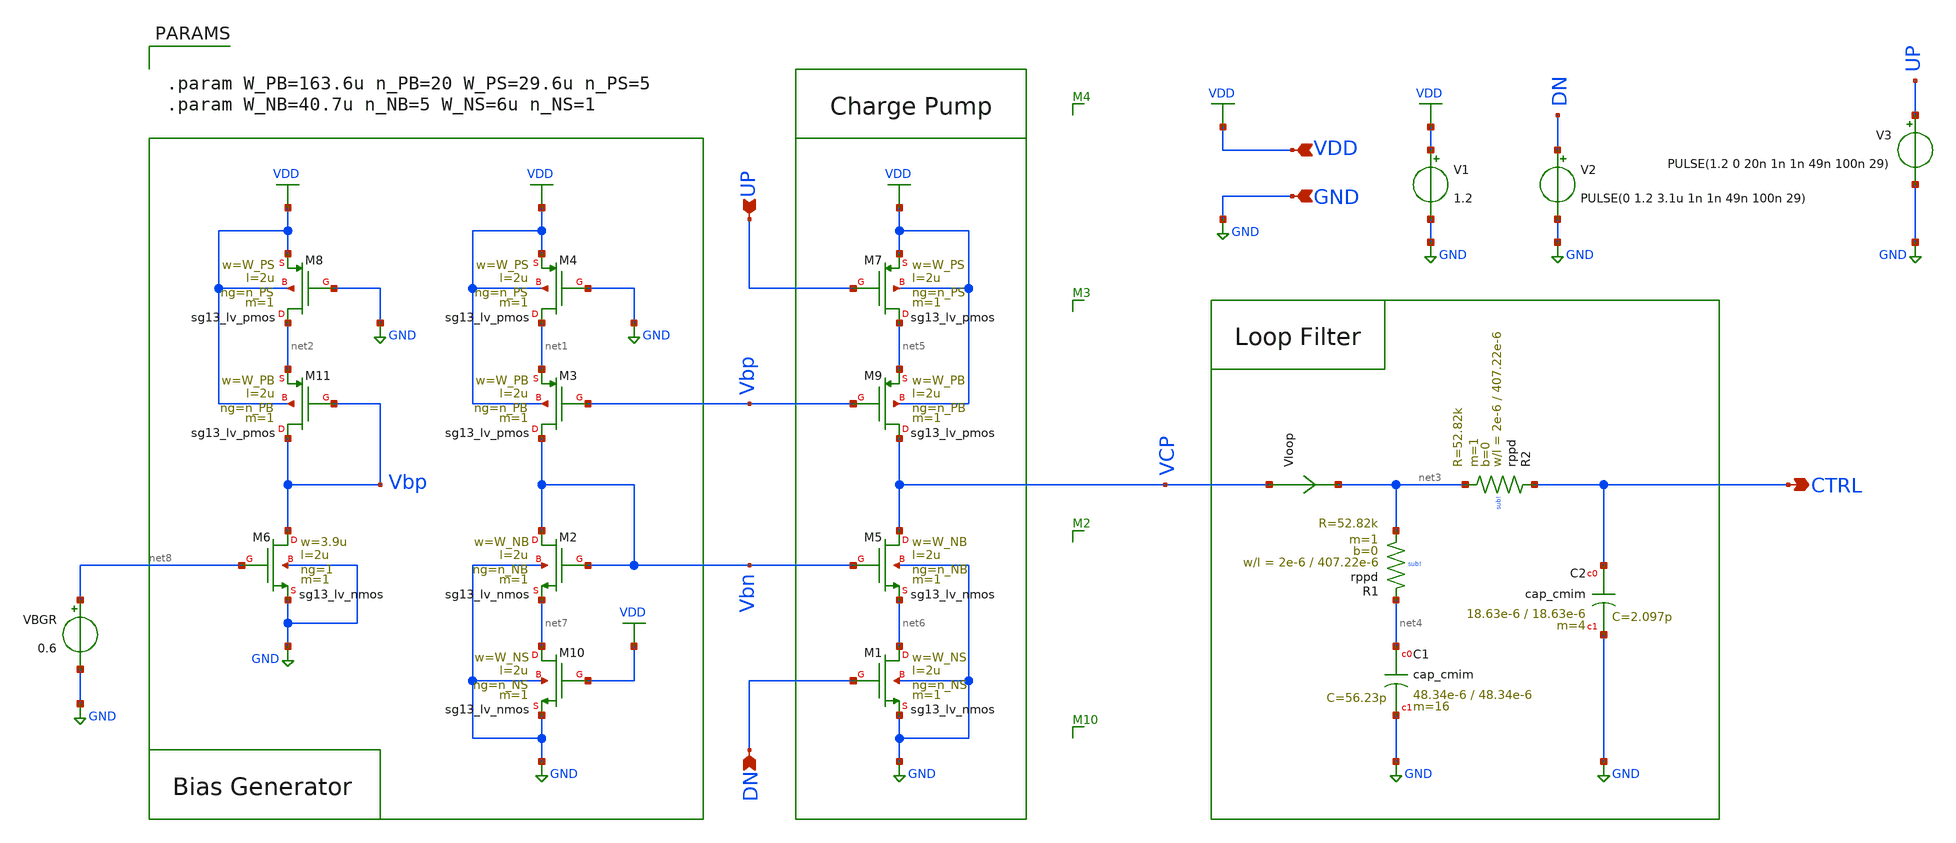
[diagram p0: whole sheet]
** sch_path: schematic/charge-pump/tb_CP.sch
**.subckt tb_CP CTRL UP VDD DN GND
*.opin CTRL
*.ipin UP
*.ipin VDD
*.ipin DN
*.ipin GND
XM2 Vbn Vbn net7 GND sg13_lv_nmos w=W_NB l=2u ng=n_NB m=1 mm_ok=1
XM8 net2 GND VDD VDD sg13_lv_pmos w=W_PS l=2u ng=n_PS m=1 mm_ok=1
XM11 Vbp Vbp net2 VDD sg13_lv_pmos w=W_PB l=2u ng=n_PB m=1 mm_ok=1
XM3 Vbn Vbp net1 VDD sg13_lv_pmos w=W_PB l=2u ng=n_PB m=1 mm_ok=1
XM4 net1 GND VDD VDD sg13_lv_pmos w=W_PS l=2u ng=n_PS m=1 mm_ok=1
XM7 net5 UP VDD VDD sg13_lv_pmos w=W_PS l=2u ng=n_PS m=1 mm_ok=1
XM9 VCP Vbp net5 VDD sg13_lv_pmos w=W_PB l=2u ng=n_PB m=1 mm_ok=1
XM10 net7 VDD GND GND sg13_lv_nmos w=W_NS l=2u ng=n_NS m=1 mm_ok=1
XM1 net6 DN GND GND sg13_lv_nmos w=W_NS l=2u ng=n_NS m=1 mm_ok=1
XM5 VCP Vbn net6 GND sg13_lv_nmos w=W_NB l=2u ng=n_NB m=1 mm_ok=1
V1 VDD GND 1.2
V2 DN GND PULSE(0 1.2 3.1u 1n 1n 49n 100n 29)
Vloop VCP net3 0
.save i(vloop)
V3 UP GND PULSE(1.2 0 20n 1n 1n 49n 100n 29)
XM6 Vbp net8 GND GND sg13_lv_nmos w=3.9u l=2u ng=1 m=1 mm_ok=1
VBGR net8 GND 0.6
XR2 CTRL net3 sub! rppd w=2e-6 l=407.22e-6 m=1 b=0 mm_ok=1
XC2 CTRL GND cap_cmim w=18.63e-6 l=18.63e-6 m=4 mm_ok=1
XR1 net4 net3 sub! rppd w=2e-6 l=407.22e-6 m=1 b=0 mm_ok=1
XC1 net4 GND cap_cmim w=48.34e-6 l=48.34e-6 m=16 mm_ok=1
**** begin user architecture code



.include tb_CP.save
.param temp=27
.option method=gear rshunt=1.0e12
.control
save all
op
write tb_CP.raw
.endc




.lib cornerMOSlv.lib mos_tt
.lib cornerMOShv.lib mos_tt
.lib cornerRES.lib res_typ
.lib cornerCAP.lib cap_typ




.param temp = 27
.options method=gear rshunt=1.0e12

.control

* Save required signals
save v(UP) v(DN) v(VCP) v(CTRL)

* Long transient simulation
tran 1n 6u

* Save raw waveform
write CP_tran.raw

* Plot transient waveform
plot v(UP) v(DN) v(VCP) v(CTRL)
plot v(CTRL)
plot i(Vloop)
plot v(vbp) v(vbn)

.endc





.param W_PB=163.6u n_PB=20 W_PS=29.6u n_PS=5
.param W_NB=40.7u n_NB=5 W_NS=6u n_NS=1


**** end user architecture code
**.ends
.GLOBAL GND
.GLOBAL VDD
.end
